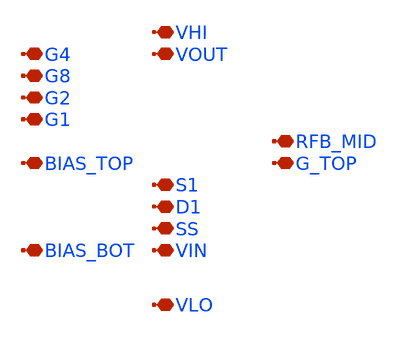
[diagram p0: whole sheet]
** sch_path: xschem/LNA_complete_2_wo_ind_PEX_old1.sch
**.subckt LNA_complete_2_wo_ind_PEX_old1 VHI VLO VOUT VIN SS D1 S1 BIAS_BOT BIAS_TOP G_TOP G2 G8 G4
*+ G1 RFB_MID
*.iopin VHI
*.iopin VLO
*.iopin VOUT
*.iopin VIN
*.iopin SS
*.iopin D1
*.iopin S1
*.iopin BIAS_BOT
*.iopin BIAS_TOP
*.iopin G_TOP
*.iopin G2
*.iopin G8
*.iopin G4
*.iopin G1
*.iopin RFB_MID
**** begin user architecture code

X0 S1 G_TOP VOUT VLO sky130_fd_pr__nfet_01v8 ad=9.898e+12p pd=7.462e+07u as=1.414e+13p ps=1.066e+08u
+ w=5.05e+06u l=150000u
X1 SS VIN D1 VLO sky130_fd_pr__nfet_01v8 ad=5.656e+12p pd=4.264e+07u as=7.07e+12p ps=5.33e+07u
+ w=5.05e+06u l=150000u
X2 VHI VLO sky130_fd_pr__cap_mim_m3_2 l=4.4e+07u w=5e+07u
X3 VOUT G_TOP S1 VLO sky130_fd_pr__nfet_01v8 ad=0p pd=0u as=0p ps=0u w=5.05e+06u l=150000u
X4 SS VIN D1 VLO sky130_fd_pr__nfet_01v8 ad=0p pd=0u as=0p ps=0u w=5.05e+06u l=150000u
X5 D1 VIN SS VLO sky130_fd_pr__nfet_01v8 ad=0p pd=0u as=0p ps=0u w=5.05e+06u l=150000u
X6 VHI a_n6328_16092# sky130_fd_pr__cap_mim_m3_1 l=2e+06u w=2.5e+06u
X7 D1 VIN SS VLO sky130_fd_pr__nfet_01v8 ad=0p pd=0u as=0p ps=0u w=5.05e+06u l=150000u
R0 BIAS_TOP G_TOP sky130_fd_pr__res_generic_po w=330000u l=1.28e+07u
X8 S1 G_TOP VOUT VLO sky130_fd_pr__nfet_01v8 ad=0p pd=0u as=0p ps=0u w=5.05e+06u l=150000u
X9 SS VIN D1 VLO sky130_fd_pr__nfet_01v8 ad=0p pd=0u as=0p ps=0u w=5.05e+06u l=150000u
X10 D1 VIN SS VLO sky130_fd_pr__nfet_01v8 ad=0p pd=0u as=0p ps=0u w=5.05e+06u l=150000u
X11 VLO VHI sky130_fd_pr__cap_mim_m3_1 l=4.4e+07u w=5e+07u
X12 BIAS_TOP VLO sky130_fd_pr__cap_mim_m3_2 l=7.5e+06u w=4.5e+06u
X13 VIN VLO sky130_fd_pr__cap_mim_m3_2 l=1.15e+07u w=9.5e+06u
X14 S1 G_TOP VOUT VLO sky130_fd_pr__nfet_01v8 ad=0p pd=0u as=0p ps=0u w=5.05e+06u l=150000u
X15 VOUT G_TOP S1 VLO sky130_fd_pr__nfet_01v8 ad=0p pd=0u as=0p ps=0u w=5.05e+06u l=150000u
X16 D1 VIN SS VLO sky130_fd_pr__nfet_01v8 ad=0p pd=0u as=0p ps=0u w=5.05e+06u l=150000u
X17 VOUT G_TOP S1 VLO sky130_fd_pr__nfet_01v8 ad=0p pd=0u as=0p ps=0u w=5.05e+06u l=150000u
X18 VLO BIAS_TOP sky130_fd_pr__cap_mim_m3_1 l=7.5e+06u w=4.5e+06u
X19 a_n6328_16092# G1 VOUT VLO sky130_fd_pr__nfet_01v8 ad=2.828e+12p pd=2.132e+07u as=0p ps=0u
+ w=5.05e+06u l=150000u
X20 a_n5540_16092# G4 VOUT VLO sky130_fd_pr__nfet_01v8 ad=2.828e+12p pd=2.132e+07u as=0p ps=0u
+ w=5.05e+06u l=150000u
X21 S1 G_TOP VOUT VLO sky130_fd_pr__nfet_01v8 ad=0p pd=0u as=0p ps=0u w=5.05e+06u l=150000u
R1 RFB_MID VOUT sky130_fd_pr__res_generic_po w=330000u l=1.28e+07u
X22 VOUT G2 a_n6722_16092# VLO sky130_fd_pr__nfet_01v8 ad=0p pd=0u as=2.828e+12p ps=2.132e+07u
+ w=5.05e+06u l=150000u
X23 VOUT G8 a_n5934_16092# VLO sky130_fd_pr__nfet_01v8 ad=0p pd=0u as=2.828e+12p ps=2.132e+07u
+ w=5.05e+06u l=150000u
X24 VOUT G_TOP S1 VLO sky130_fd_pr__nfet_01v8 ad=0p pd=0u as=0p ps=0u w=5.05e+06u l=150000u
X25 VLO VIN sky130_fd_pr__cap_mim_m3_1 l=1.15e+07u w=9.5e+06u
X26 S1 G_TOP VOUT VLO sky130_fd_pr__nfet_01v8 ad=0p pd=0u as=0p ps=0u w=5.05e+06u l=150000u
X27 VOUT G_TOP S1 VLO sky130_fd_pr__nfet_01v8 ad=0p pd=0u as=0p ps=0u w=5.05e+06u l=150000u
X28 VOUT G_TOP S1 VLO sky130_fd_pr__nfet_01v8 ad=0p pd=0u as=0p ps=0u w=5.05e+06u l=150000u
X29 S1 G_TOP VOUT VLO sky130_fd_pr__nfet_01v8 ad=0p pd=0u as=0p ps=0u w=5.05e+06u l=150000u
X30 VHI a_n5934_16092# sky130_fd_pr__cap_mim_m3_1 l=5e+06u w=8e+06u
X31 VIN RFB_MID sky130_fd_pr__cap_mim_m3_2 l=2.05e+07u w=1.15e+07u
X32 VOUT G1 a_n6328_16092# VLO sky130_fd_pr__nfet_01v8 ad=0p pd=0u as=0p ps=0u w=5.05e+06u l=150000u
X33 VOUT G4 a_n5540_16092# VLO sky130_fd_pr__nfet_01v8 ad=0p pd=0u as=0p ps=0u w=5.05e+06u l=150000u
X34 a_n5934_16092# G8 VOUT VLO sky130_fd_pr__nfet_01v8 ad=0p pd=0u as=0p ps=0u w=5.05e+06u l=150000u
R2 BIAS_BOT VIN sky130_fd_pr__res_generic_po w=330000u l=2.068e+07u
X35 RFB_MID VIN sky130_fd_pr__cap_mim_m3_1 l=2.05e+07u w=1.15e+07u
X36 VHI a_n5540_16092# sky130_fd_pr__cap_mim_m3_1 l=5e+06u w=4e+06u
X37 VHI a_n6722_16092# sky130_fd_pr__cap_mim_m3_1 l=4e+06u w=2.5e+06u
X38 a_n6722_16092# G2 VOUT VLO sky130_fd_pr__nfet_01v8 ad=0p pd=0u as=0p ps=0u w=5.05e+06u l=150000u
X39 SS VIN D1 VLO sky130_fd_pr__nfet_01v8 ad=0p pd=0u as=0p ps=0u w=5.05e+06u l=150000u
C0 G_TOP S1 1.40fF
C1 VIN RFB_MID 40.52fF
C2 VHI a_n5540_16092# 2.49fF
C3 G_TOP VOUT 2.66fF
C4 a_n5540_16092# VOUT 3.94fF
C5 VIN SS 7.60fF
C6 VHI a_n5934_16092# 4.77fF
C7 a_n5934_16092# VOUT 4.73fF
C8 S1 VOUT 20.16fF
C9 VHI a_n6722_16092# 1.71fF
C10 a_n6722_16092# VOUT 3.54fF
C11 D1 VIN 1.74fF
C12 VHI VOUT 1.26fF
C13 m5_n800_n3000# SS 4.96fF
C14 VHI a_n6328_16092# 1.11fF
C15 VOUT a_n6328_16092# 3.57fF
C16 D1 SS 13.20fF
C17 VHI VLO 422.33fF
C18 SS VLO 9.48fF
C19 D1 VLO 14.87fF
C20 VIN VLO 47.34fF
C21 RFB_MID VLO 5.70fF
C22 S1 VLO 14.45fF
C23 BIAS_TOP VLO 14.09fF
C24 G_TOP VLO 4.04fF
C25 a_n5540_16092# VLO 3.87fF
C26 a_n5934_16092# VLO 3.33fF
C27 a_n6328_16092# VLO 3.14fF
C28 VOUT VLO 53.05fF
C29 a_n6722_16092# VLO 3.39fF
C30 G4 VLO 1.28fF
C31 G8 VLO 1.10fF
C32 G1 VLO 1.06fF
C33 G2 VLO 1.29fF



**** end user architecture code
**.ends
.end
